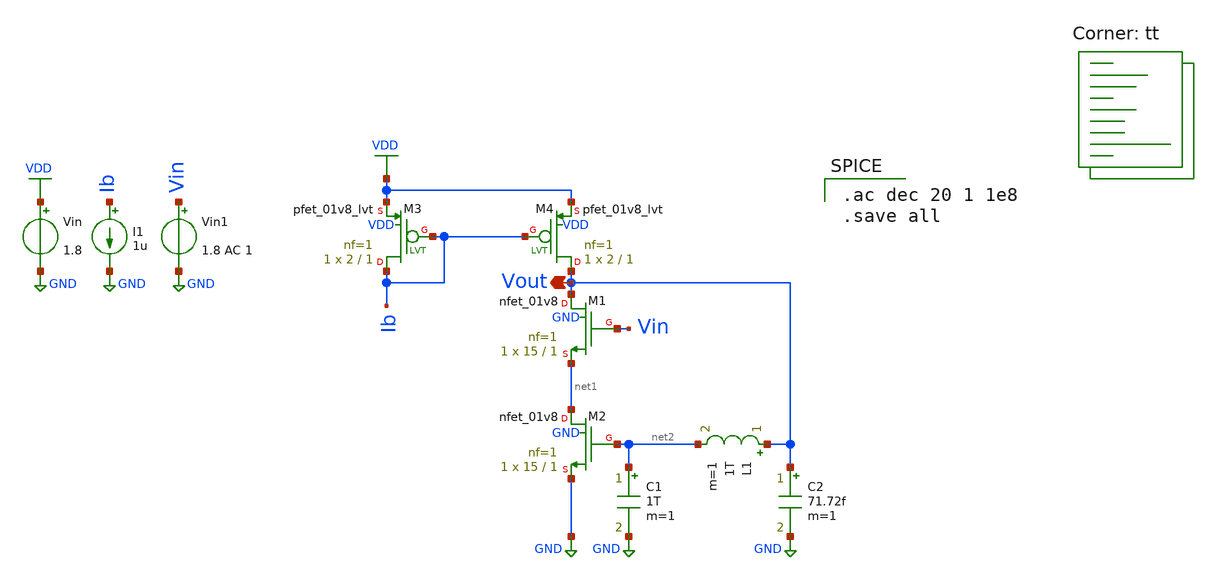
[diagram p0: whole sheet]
** sch_path: xschem/fvf_tb_loop.sch
**.subckt fvf_tb_loop Vout
*.opin Vout
Vin VDD GND 1.8
Vin1 Vin GND 1.8 AC 1
I1 Ib GND 1u
XM1 Vout Vin net1 GND sky130_fd_pr__nfet_01v8 L=1 W=15 nf=1 ad='int((nf+1)/2) * W/nf * 0.29' as='int((nf+2)/2) * W/nf * 0.29'
+ pd='2*int((nf+1)/2) * (W/nf + 0.29)' ps='2*int((nf+2)/2) * (W/nf + 0.29)' nrd='0.29 / W' nrs='0.29 / W'
+ sa=0 sb=0 sd=0 mult=1 m=1
XM2 net1 net2 GND GND sky130_fd_pr__nfet_01v8 L=1 W=15 nf=1 ad='int((nf+1)/2) * W/nf * 0.29' as='int((nf+2)/2) * W/nf * 0.29'
+ pd='2*int((nf+1)/2) * (W/nf + 0.29)' ps='2*int((nf+2)/2) * (W/nf + 0.29)' nrd='0.29 / W' nrs='0.29 / W'
+ sa=0 sb=0 sd=0 mult=1 m=1
XM3 Ib Ib VDD VDD sky130_fd_pr__pfet_01v8_lvt L=1 W=2 nf=1 ad='int((nf+1)/2) * W/nf * 0.29' as='int((nf+2)/2) * W/nf * 0.29'
+ pd='2*int((nf+1)/2) * (W/nf + 0.29)' ps='2*int((nf+2)/2) * (W/nf + 0.29)' nrd='0.29 / W' nrs='0.29 / W'
+ sa=0 sb=0 sd=0 mult=1 m=1
XM4 Vout Ib VDD VDD sky130_fd_pr__pfet_01v8_lvt L=1 W=2 nf=1 ad='int((nf+1)/2) * W/nf * 0.29' as='int((nf+2)/2) * W/nf * 0.29'
+ pd='2*int((nf+1)/2) * (W/nf + 0.29)' ps='2*int((nf+2)/2) * (W/nf + 0.29)' nrd='0.29 / W' nrs='0.29 / W'
+ sa=0 sb=0 sd=0 mult=1 m=1
L1 Vout net2 1T m=1
C1 net2 GND 1T m=1
C2 Vout GND 71.72f m=1
**** begin user architecture code
.lib $::SKYWATER_MODELS/sky130.lib.spice tt

.ac dec 20 1 1e8
.save all

**** end user architecture code
**.ends
.GLOBAL VDD
.GLOBAL GND
.end
